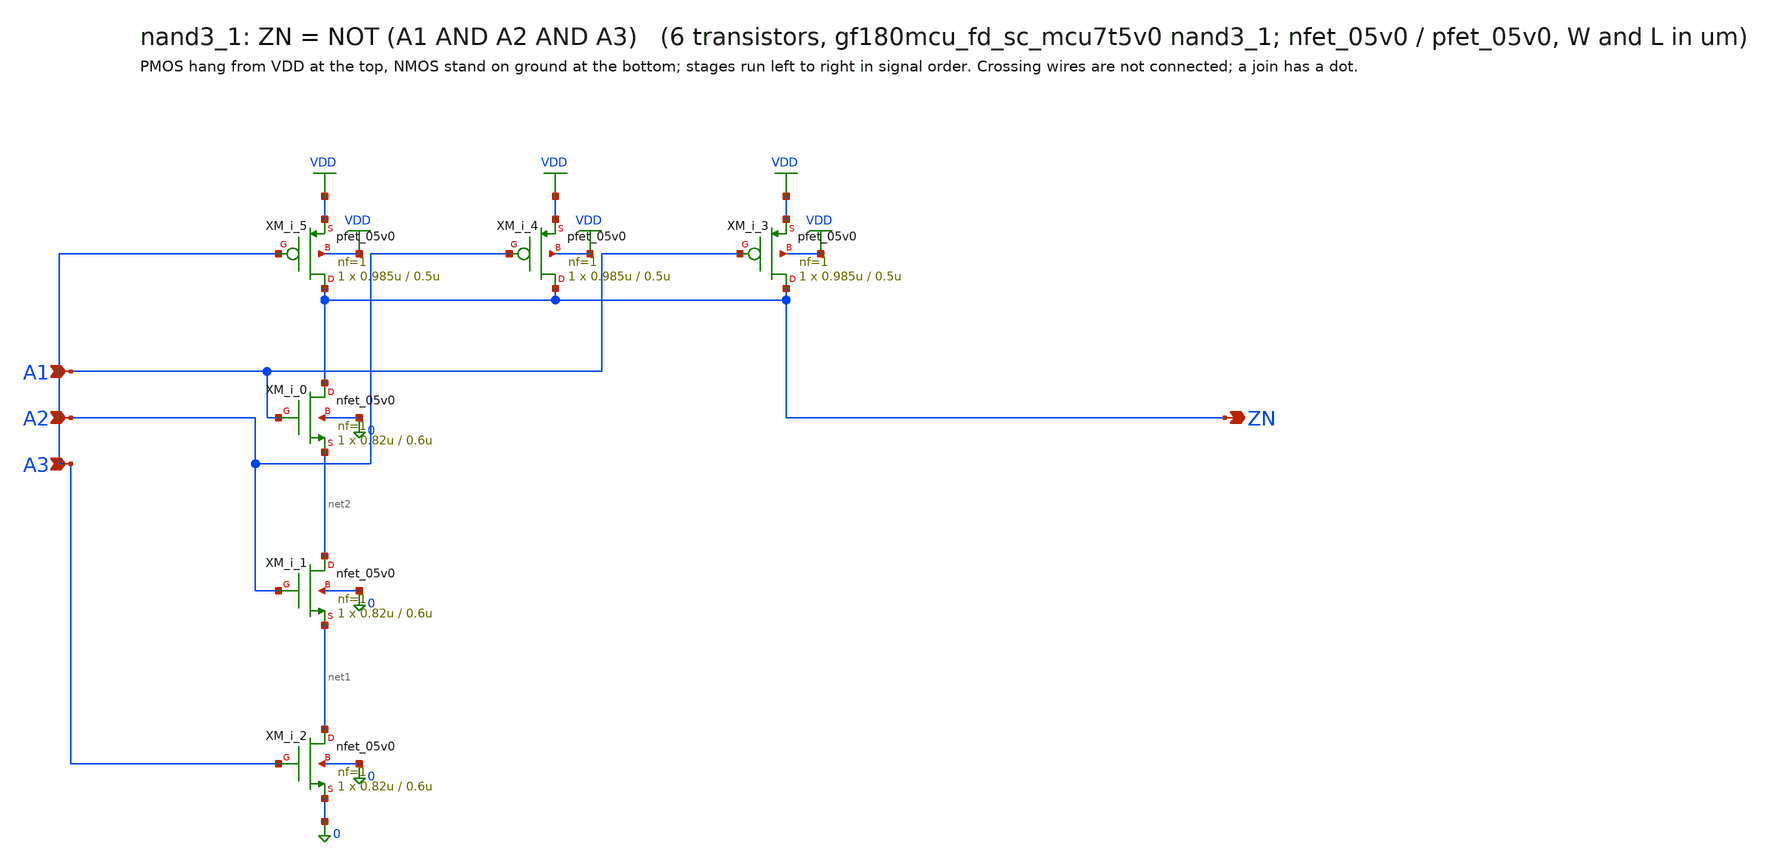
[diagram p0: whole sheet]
** sch_path: xschem/cells_tx/nand3_1.sch
**.subckt nand3_1 A1 A2 A3 ZN
*.ipin A1
*.ipin A2
*.ipin A3
*.opin ZN
XM_i_2 net1 A3 0 0 nfet_05v0 L=0.6u W=0.82u nf=1 ad=4.1e-13 as=4.1e-13 pd=2.64e-06 ps=2.64e-06 nrd=0
+ nrs=0 sa=0 sb=0 sd=0 m=1
XM_i_1 net2 A2 net1 0 nfet_05v0 L=0.6u W=0.82u nf=1 ad=4.1e-13 as=4.1e-13 pd=2.64e-06 ps=2.64e-06
+ nrd=0 nrs=0 sa=0 sb=0 sd=0 m=1
XM_i_0 ZN A1 net2 0 nfet_05v0 L=0.6u W=0.82u nf=1 ad=4.1e-13 as=4.1e-13 pd=2.64e-06 ps=2.64e-06
+ nrd=0 nrs=0 sa=0 sb=0 sd=0 m=1
XM_i_5 ZN A3 VDD VDD pfet_05v0 L=0.5u W=0.985u nf=1 ad=4.925e-13 as=4.925e-13 pd=2.97e-06
+ ps=2.97e-06 nrd=0 nrs=0 sa=0 sb=0 sd=0 m=1
XM_i_4 ZN A2 VDD VDD pfet_05v0 L=0.5u W=0.985u nf=1 ad=4.925e-13 as=4.925e-13 pd=2.97e-06
+ ps=2.97e-06 nrd=0 nrs=0 sa=0 sb=0 sd=0 m=1
XM_i_3 ZN A1 VDD VDD pfet_05v0 L=0.5u W=0.985u nf=1 ad=4.925e-13 as=4.925e-13 pd=2.97e-06
+ ps=2.97e-06 nrd=0 nrs=0 sa=0 sb=0 sd=0 m=1
**.ends
.GLOBAL VDD
.end
